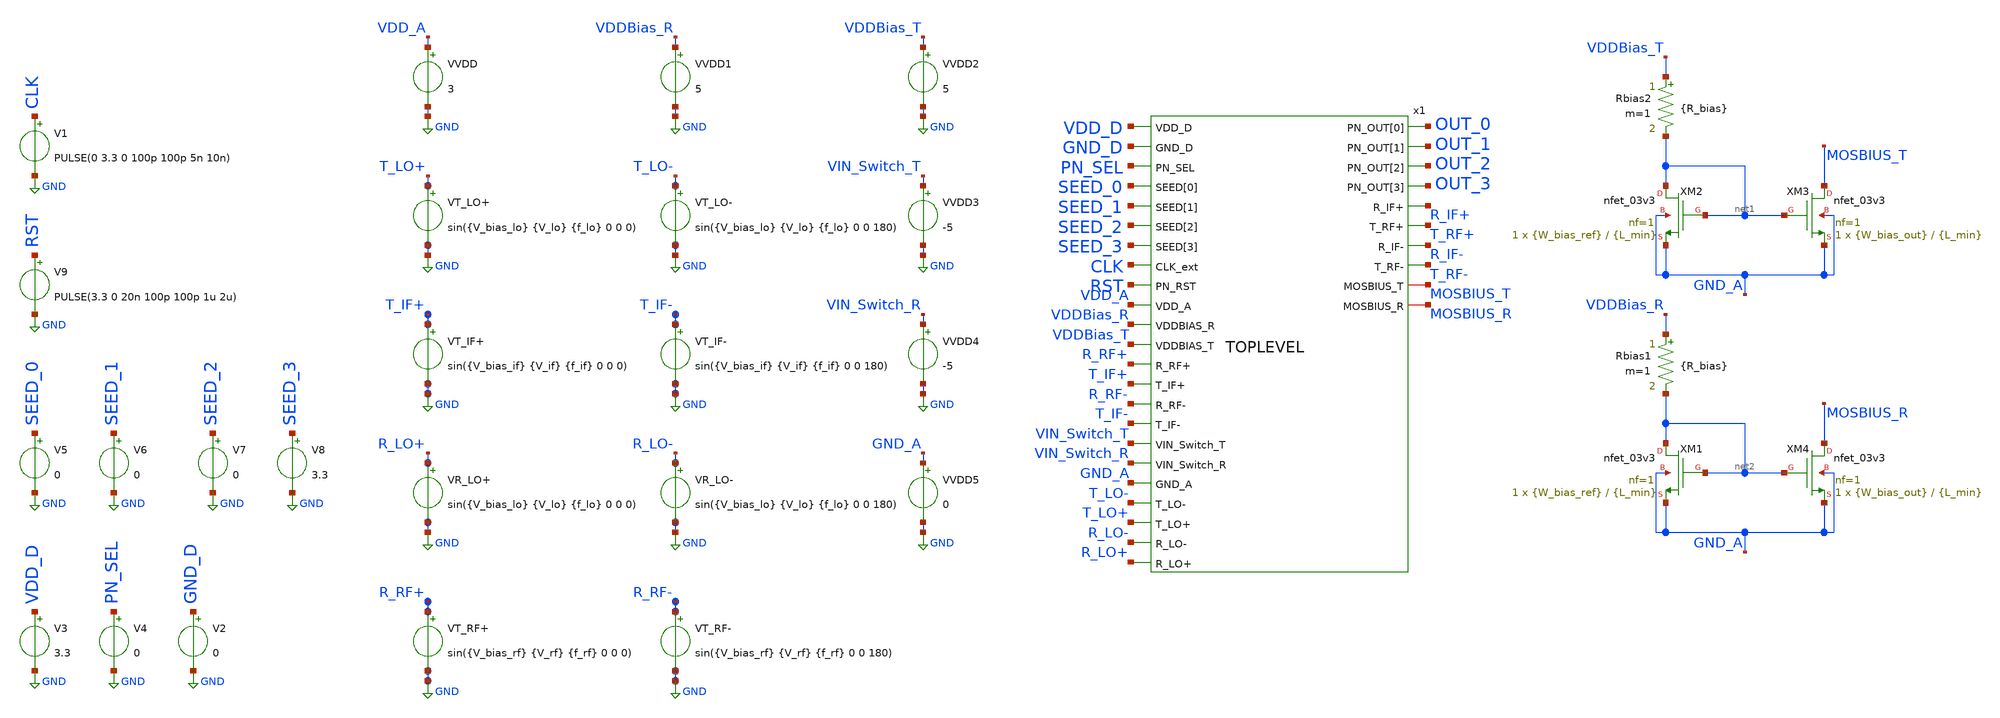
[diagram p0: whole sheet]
** sch_path: Project/1-on-chip/schematic/tb_TOPLEVEL.sch
**.subckt tb_TOPLEVEL
XM2 net1 net1 GND_A GND_A nfet_03v3 L={L_min} W={W_bias_ref} nf=1 ad='int((nf+1)/2) * W/nf * 0.18u' as='int((nf+2)/2) * W/nf * 0.18u'
+ pd='2*int((nf+1)/2) * (W/nf + 0.18u)' ps='2*int((nf+2)/2) * (W/nf + 0.18u)' nrd='0.18u / W' nrs='0.18u / W'
+ sa=0 sb=0 sd=0 m=1
XM3 MOSBIUS_T net1 GND_A GND_A nfet_03v3 L={L_min} W={W_bias_out} nf=1 ad='int((nf+1)/2) * W/nf * 0.18u'
+ as='int((nf+2)/2) * W/nf * 0.18u' pd='2*int((nf+1)/2) * (W/nf + 0.18u)' ps='2*int((nf+2)/2) * (W/nf + 0.18u)'
+ nrd='0.18u / W' nrs='0.18u / W' sa=0 sb=0 sd=0 m=1
Rbias2 VDDBias_T net1 {R_bias} m=1
XM1 net2 net2 GND_A GND_A nfet_03v3 L={L_min} W={W_bias_ref} nf=1 ad='int((nf+1)/2) * W/nf * 0.18u' as='int((nf+2)/2) * W/nf * 0.18u'
+ pd='2*int((nf+1)/2) * (W/nf + 0.18u)' ps='2*int((nf+2)/2) * (W/nf + 0.18u)' nrd='0.18u / W' nrs='0.18u / W'
+ sa=0 sb=0 sd=0 m=1
XM4 MOSBIUS_R net2 GND_A GND_A nfet_03v3 L={L_min} W={W_bias_out} nf=1 ad='int((nf+1)/2) * W/nf * 0.18u'
+ as='int((nf+2)/2) * W/nf * 0.18u' pd='2*int((nf+1)/2) * (W/nf + 0.18u)' ps='2*int((nf+2)/2) * (W/nf + 0.18u)'
+ nrd='0.18u / W' nrs='0.18u / W' sa=0 sb=0 sd=0 m=1
Rbias1 VDDBias_R net2 {R_bias} m=1
VVDD VDD_A GND 3
VT_LO+ T_LO+ GND sin({V_bias_lo} {V_lo} {f_lo} 0 0 0)
VT_LO- T_LO- GND sin({V_bias_lo} {V_lo} {f_lo} 0 0 180)
VT_IF+ T_IF+ GND sin({V_bias_if} {V_if} {f_if} 0 0 0)
VT_IF- T_IF- GND sin({V_bias_if} {V_if} {f_if} 0 0 180)
VR_LO+ R_LO+ GND sin({V_bias_lo} {V_lo} {f_lo} 0 0 0)
VR_LO- R_LO- GND sin({V_bias_lo} {V_lo} {f_lo} 0 0 180)
VT_RF+ R_RF+ GND sin({V_bias_rf} {V_rf} {f_rf} 0 0 0)
VT_RF- R_RF- GND sin({V_bias_rf} {V_rf} {f_rf} 0 0 180)
VVDD1 VDDBias_R GND 5
V1 CLK GND PULSE(0 3.3 0 100p 100p 5n 10n)
V3 VDD_D GND 3.3
V4 PN_SEL GND 0
V5 SEED_0 GND 0
V6 SEED_1 GND 0
V7 SEED_2 GND 0
V8 SEED_3 GND 3.3
V9 RST GND PULSE(3.3 0 20n 100p 100p 1u 2u)
V2 GND_D GND 0
VVDD2 VDDBias_T GND 5
VVDD3 VIN_Switch_T GND -5
VVDD4 VIN_Switch_R GND -5
VVDD5 GND_A GND 0
x1 OUT_0 VDD_D GND_D OUT_1 PN_SEL OUT_2 OUT_3 SEED_0 SEED_1 SEED_2 SEED_3 CLK RST VDD_A VDDBias_R
+ VDDBias_T R_RF+ T_IF+ R_IF+ T_RF+ R_RF- T_IF- R_IF- T_RF- MOSBIUS_T MOSBIUS_R VIN_Switch_T VIN_Switch_R GND_A
+ T_LO- T_LO+ R_LO- R_LO+ TOPLEVEL
**** begin user architecture code

.include /foss/pdks/gf180mcuD/libs.tech/ngspice/design.ngspice
.lib /foss/pdks/gf180mcuD/libs.tech/ngspice/sm141064.ngspice typical



**** begin user architecture code
* Run transient analysis
.tran 1n 200n

* control
.control
    run
    set hcopydevtype=postscript
    set hcopypscolor=1
    plot v(RST) v(CLK)+4 v(OUT_3)+8 v(OUT_2)+12 v(OUT_1)+16 v(OUT_0)+20
.endc

.end

**** end user architecture code




.tran 200p 800n

.control
run
  * UPCONVERSION (WORKING since the RF IF change roles when upconversion)
plot (V(T_IF+)-V(T_IF-)) V(T_LO+)-V(T_LO-)+2 (V(T_RF+)-V(T_RF-))+4
plot mag(fft(V(T_RF+) - V(T_RF-)))

  * DOWNCONVERSION
plot (V(R_IF+)-V(R_IF-)) V(R_LO+)-V(R_LO-)+2 (V(R_RF+)-V(R_RF-))+4
plot mag(fft(V(R_IF+) - V(R_IF-)))
.endc




* --- Parameters for the Testbench ---

* --- Supply ---
.param V_VDD = 3.3V

* --- Signal Sources ---

// LO from VCO+PLL
.param V_bias_lo = 1.2V
.param V_lo = 0.5V
.param f_lo = 50MEG

// RF Input for Receiver
.param V_bias_rf = 1.2V
.param V_rf = 0.063V
.param f_rf = 60MEG

// IF Input for Transmitter
.param V_bias_if = 1.2V
.param V_if = 0.5V
.param f_if = 10MEG

// External Current Mirror
.param L_min = 0.28u
.param WL_bias_ref_ratio = 10
.param WL_bias_out_ratio = 60
.param W_bias_ref = {WL_bias_ref_ratio * L_min}
.param W_bias_out = {WL_bias_out_ratio * L_min}
.param R_bias = 7.5k


**** end user architecture code
**.ends
.GLOBAL GND
.end
